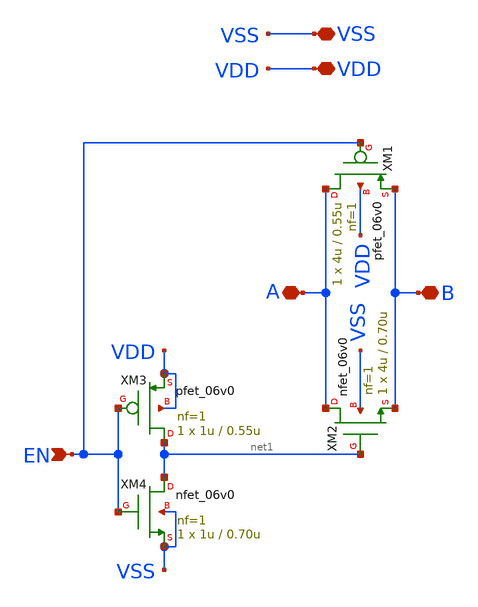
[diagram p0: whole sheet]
** sch_path: analog/xschem/trans.sch
**.subckt trans VSS VDD EN B A
*.iopin VSS
*.iopin VDD
*.ipin EN
*.iopin B
*.iopin A
XM1 A EN B VDD pfet_06v0 L=0.55u W=4u nf=1 ad='int((nf+1)/2) * W/nf * 0.18u' as='int((nf+2)/2) * W/nf * 0.18u'
+ pd='2*int((nf+1)/2) * (W/nf + 0.18u)' ps='2*int((nf+2)/2) * (W/nf + 0.18u)' nrd='0.18u / W' nrs='0.18u / W'
+ sa=0 sb=0 sd=0 m=1
XM2 A net1 B VSS nfet_06v0 L=0.70u W=4u nf=1 ad='int((nf+1)/2) * W/nf * 0.18u' as='int((nf+2)/2) * W/nf * 0.18u'
+ pd='2*int((nf+1)/2) * (W/nf + 0.18u)' ps='2*int((nf+2)/2) * (W/nf + 0.18u)' nrd='0.18u / W' nrs='0.18u / W'
+ sa=0 sb=0 sd=0 m=1
XM3 net1 EN VDD VDD pfet_06v0 L=0.55u W=1u nf=1 ad='int((nf+1)/2) * W/nf * 0.18u' as='int((nf+2)/2) * W/nf * 0.18u'
+ pd='2*int((nf+1)/2) * (W/nf + 0.18u)' ps='2*int((nf+2)/2) * (W/nf + 0.18u)' nrd='0.18u / W' nrs='0.18u / W'
+ sa=0 sb=0 sd=0 m=1
XM4 net1 EN VSS VSS nfet_06v0 L=0.70u W=1u nf=1 ad='int((nf+1)/2) * W/nf * 0.18u' as='int((nf+2)/2) * W/nf * 0.18u'
+ pd='2*int((nf+1)/2) * (W/nf + 0.18u)' ps='2*int((nf+2)/2) * (W/nf + 0.18u)' nrd='0.18u / W' nrs='0.18u / W'
+ sa=0 sb=0 sd=0 m=1
**.ends
.end
